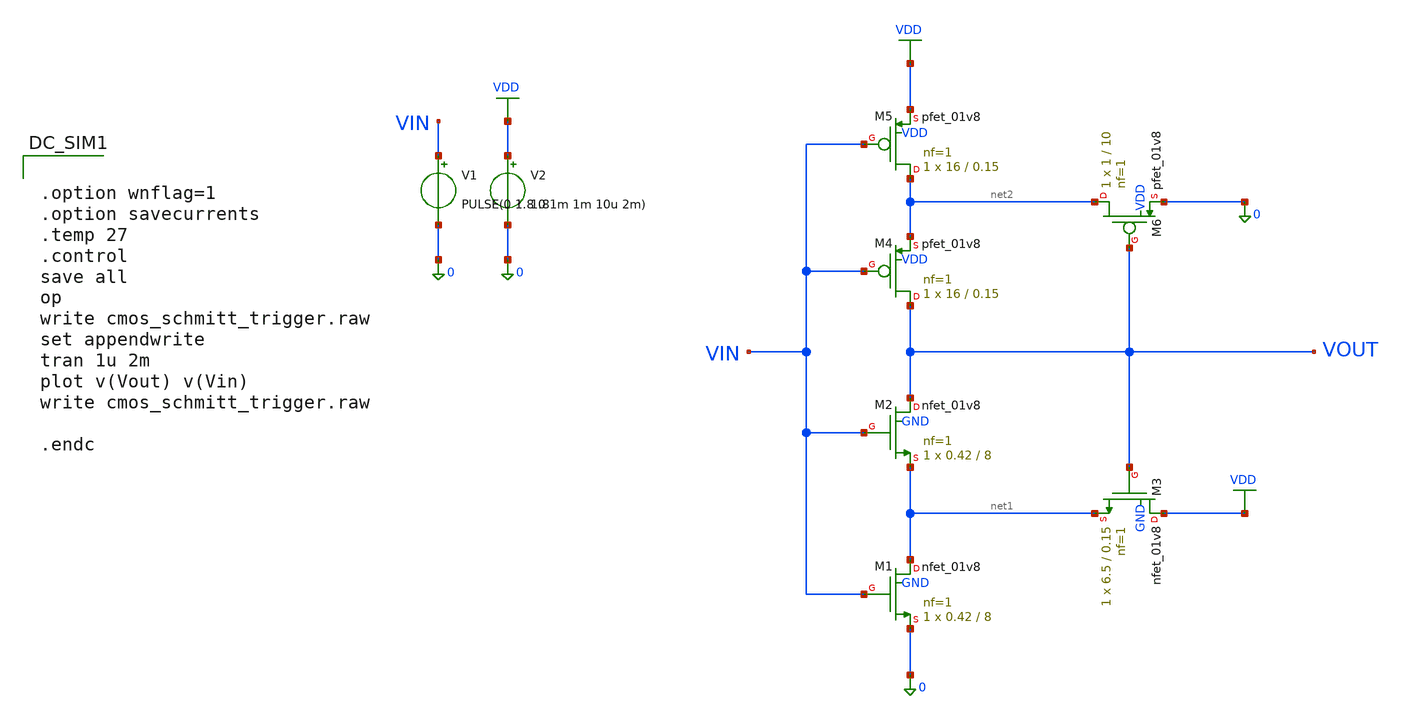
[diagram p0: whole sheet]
** sch_path: POR_V2/cmos_schmitt_trigger.sch
**.subckt cmos_schmitt_trigger
XM1 net1 VIN 0 GND sky130_fd_pr__nfet_01v8 L=8 W=0.42 nf=1 ad='int((1 + 1)/2) * 0.42 / 1 * 0.29' as='int((1 + 2)/2) * 0.42 / 1 * 0.29'
+ pd='2*int((1 + 1)/2) * (0.42 / 1 + 0.29)' ps='2*int((1 + 2)/2) * (0.42 / 1 + 0.29)' nrd='0.29 / 0.42 '
+ nrs='0.29 / 0.42 ' sa=0 sb=0 sd=0 mult=1 m=1
XM2 VOUT VIN net1 GND sky130_fd_pr__nfet_01v8 L=8 W=0.42 nf=1 ad='int((1 + 1)/2) * 0.42 / 1 * 0.29' as='int((1 + 2)/2) * 0.42 / 1 * 0.29'
+ pd='2*int((1 + 1)/2) * (0.42 / 1 + 0.29)' ps='2*int((1 + 2)/2) * (0.42 / 1 + 0.29)' nrd='0.29 / 0.42 '
+ nrs='0.29 / 0.42 ' sa=0 sb=0 sd=0 mult=1 m=1
XM3 VDD VOUT net1 GND sky130_fd_pr__nfet_01v8 L=0.15 W=6.5 nf=1 ad='int((1 + 1)/2) * 6.5 / 1 * 0.29'
+ as='int((1 + 2)/2) * 6.5 / 1 * 0.29' pd='2*int((1 + 1)/2) * (6.5 / 1 + 0.29)' ps='2*int((1 + 2)/2) * (6.5 / 1 + 0.29)'
+ nrd='0.29 / 6.5 ' nrs='0.29 / 6.5 ' sa=0 sb=0 sd=0 mult=1 m=1
XM4 VOUT VIN net2 VDD sky130_fd_pr__pfet_01v8 L=0.15 W=16 nf=1 ad='int((1 + 1)/2) * 16 / 1 * 0.29' as='int((1 + 2)/2) * 16 / 1 * 0.29'
+ pd='2*int((1 + 1)/2) * (16 / 1 + 0.29)' ps='2*int((1 + 2)/2) * (16 / 1 + 0.29)' nrd='0.29 / 16 ' nrs='0.29 / 16 '
+ sa=0 sb=0 sd=0 mult=1 m=1
XM5 net2 VIN VDD VDD sky130_fd_pr__pfet_01v8 L=0.15 W=16 nf=1 ad='int((1 + 1)/2) * 16 / 1 * 0.29' as='int((1 + 2)/2) * 16 / 1 * 0.29'
+ pd='2*int((1 + 1)/2) * (16 / 1 + 0.29)' ps='2*int((1 + 2)/2) * (16 / 1 + 0.29)' nrd='0.29 / 16 ' nrs='0.29 / 16 '
+ sa=0 sb=0 sd=0 mult=1 m=1
XM6 net2 VOUT 0 VDD sky130_fd_pr__pfet_01v8 L=10 W=1 nf=1 ad='int((1 + 1)/2) * 1 / 1 * 0.29' as='int((1 + 2)/2) * 1 / 1 * 0.29'
+ pd='2*int((1 + 1)/2) * (1 / 1 + 0.29)' ps='2*int((1 + 2)/2) * (1 / 1 + 0.29)' nrd='0.29 / 1 ' nrs='0.29 / 1 '
+ sa=0 sb=0 sd=0 mult=1 m=1
V2 VDD 0 1.8
V1 VIN 0 PULSE(0 1.8 0 1m 1m 10u 2m)
**** begin user architecture code

** opencircuitdesign pdks install
.lib $::SKYWATER_MODELS/sky130.lib.spice tt



.option wnflag=1
.option savecurrents
.temp 27
.control
save all
op
write cmos_schmitt_trigger.raw
set appendwrite
tran 1u 2m
plot v(Vout) v(Vin)
write cmos_schmitt_trigger.raw

.endc


**** end user architecture code
**.ends
.GLOBAL VDD
.end
